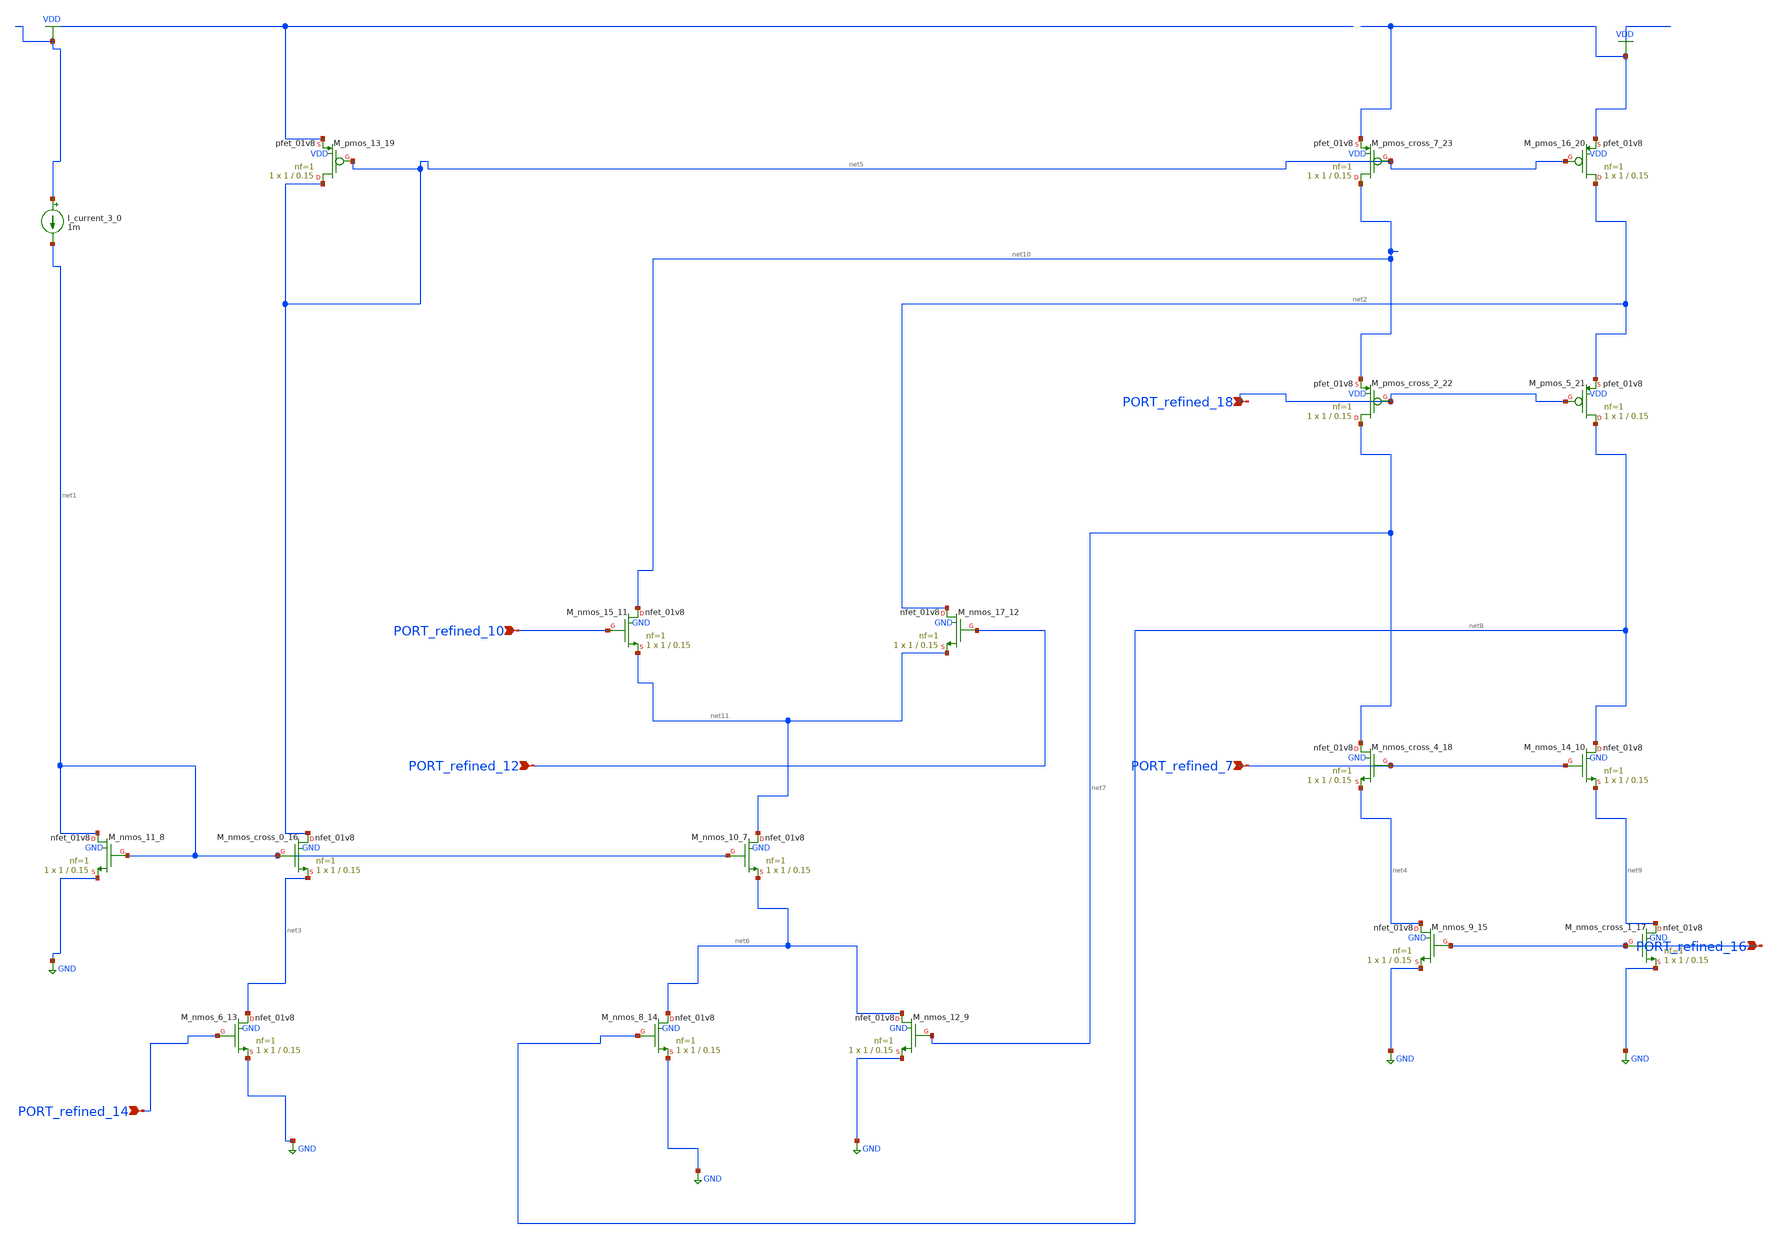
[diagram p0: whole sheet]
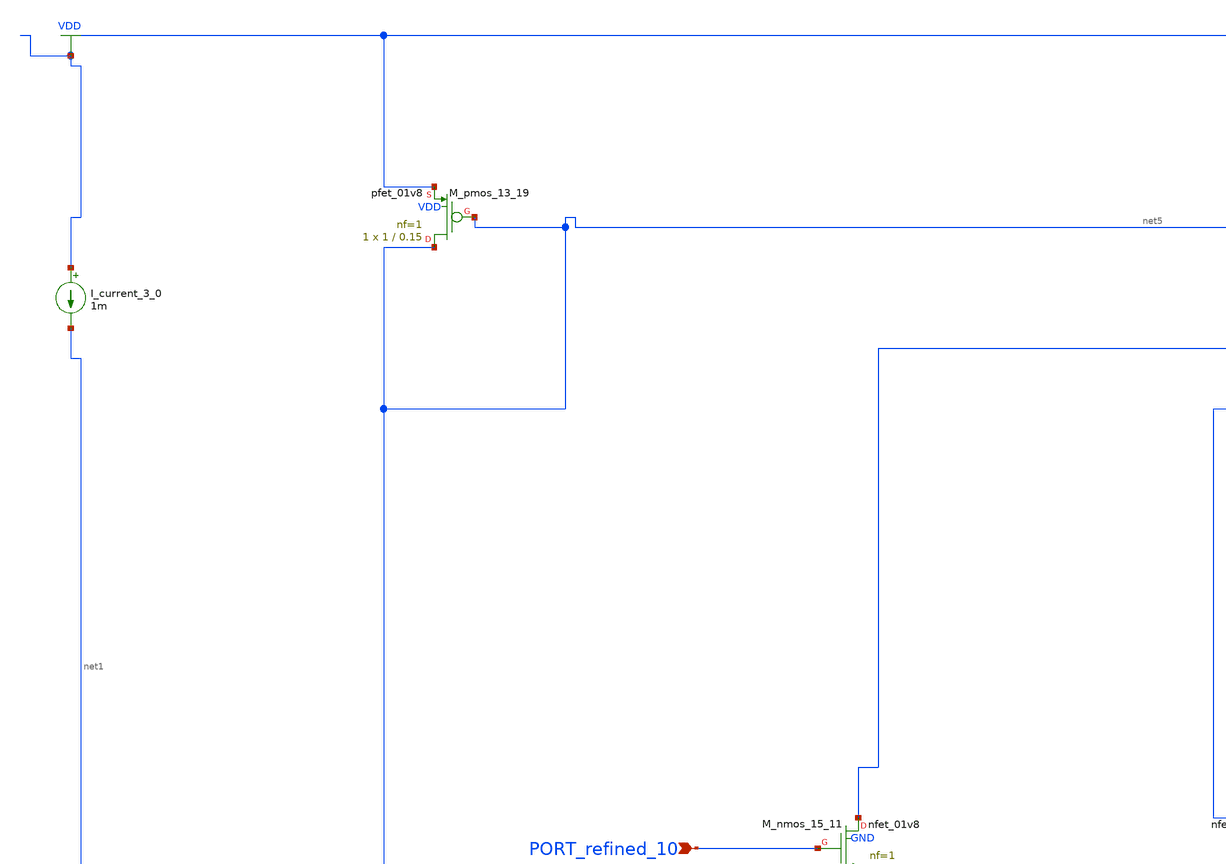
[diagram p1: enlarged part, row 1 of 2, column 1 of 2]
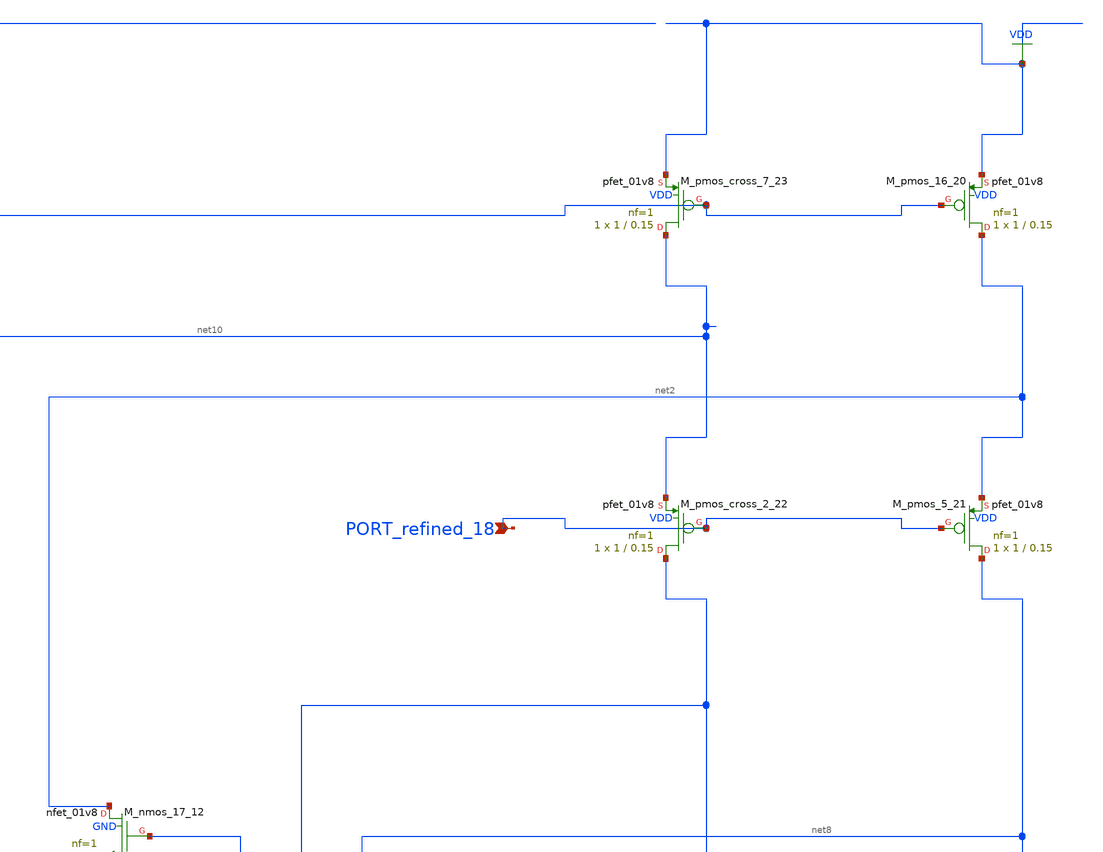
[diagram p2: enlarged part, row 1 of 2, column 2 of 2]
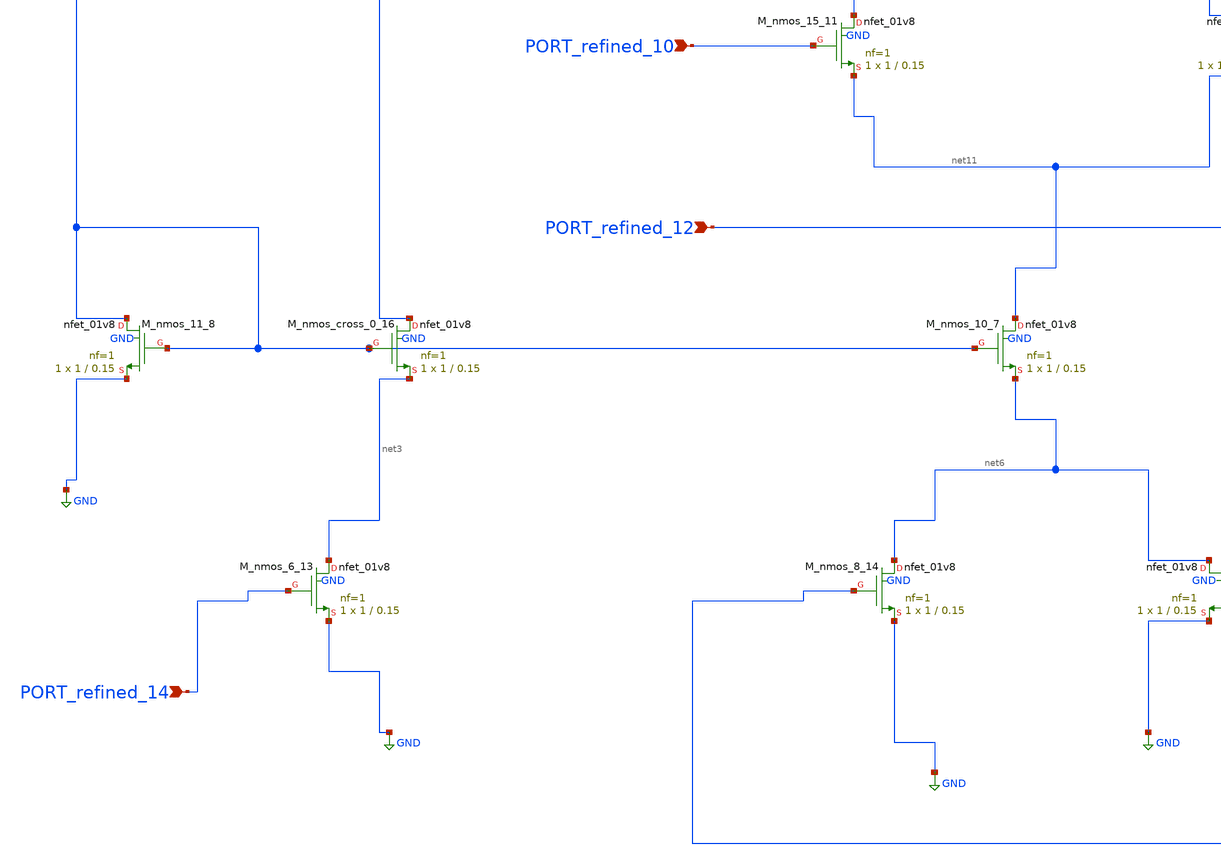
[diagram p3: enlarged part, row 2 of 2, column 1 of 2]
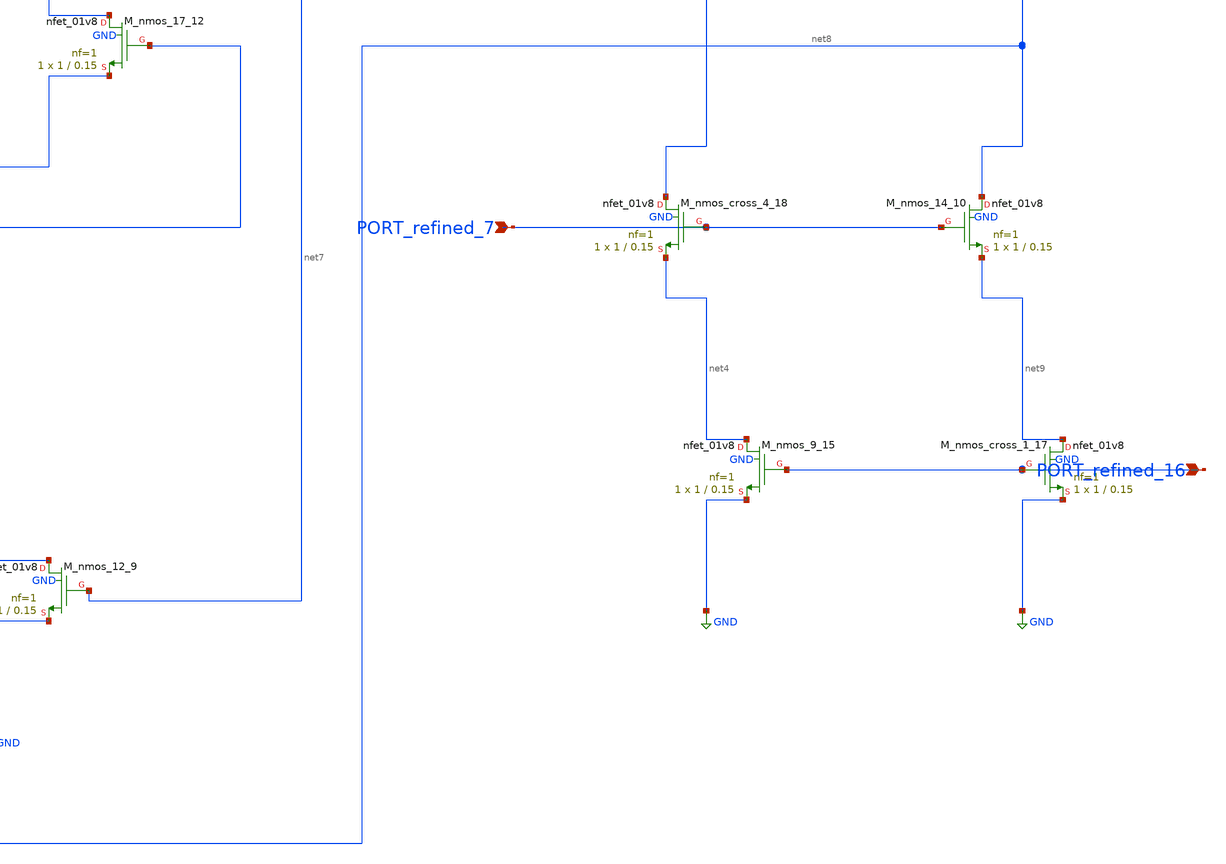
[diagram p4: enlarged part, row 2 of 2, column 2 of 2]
** sch_path: schematics/AMSNet/672.sch
**.subckt 672 PORT_refined_12 PORT_refined_14 PORT_refined_7 PORT_refined_16 PORT_refined_18
*+ PORT_refined_10
*.ipin PORT_refined_12
*.ipin PORT_refined_14
*.ipin PORT_refined_7
*.ipin PORT_refined_16
*.ipin PORT_refined_18
*.ipin PORT_refined_10
I_current_3_0 VDD net1 1m
XM_nmos_10_7 net11 net1 net6 GND sky130_fd_pr__nfet_01v8 L=0.15 W=1 nf=1 ad='int((1 + 1)/2) * 1 / 1 * 0.29'
+ as='int((1 + 2)/2) * 1 / 1 * 0.29' pd='2*int((1 + 1)/2) * (1 / 1 + 0.29)' ps='2*int((1 + 2)/2) * (1 / 1 + 0.29)'
+ nrd='0.29 / 1 ' nrs='0.29 / 1 ' sa=0 sb=0 sd=0 mult=1 m=1
XM_nmos_11_8 net1 net1 GND GND sky130_fd_pr__nfet_01v8 L=0.15 W=1 nf=1 ad='int((1 + 1)/2) * 1 / 1 * 0.29'
+ as='int((1 + 2)/2) * 1 / 1 * 0.29' pd='2*int((1 + 1)/2) * (1 / 1 + 0.29)' ps='2*int((1 + 2)/2) * (1 / 1 + 0.29)'
+ nrd='0.29 / 1 ' nrs='0.29 / 1 ' sa=0 sb=0 sd=0 mult=1 m=1
XM_nmos_12_9 net6 net7 GND GND sky130_fd_pr__nfet_01v8 L=0.15 W=1 nf=1 ad='int((1 + 1)/2) * 1 / 1 * 0.29'
+ as='int((1 + 2)/2) * 1 / 1 * 0.29' pd='2*int((1 + 1)/2) * (1 / 1 + 0.29)' ps='2*int((1 + 2)/2) * (1 / 1 + 0.29)'
+ nrd='0.29 / 1 ' nrs='0.29 / 1 ' sa=0 sb=0 sd=0 mult=1 m=1
XM_nmos_14_10 net8 PORT_refined_7 net9 GND sky130_fd_pr__nfet_01v8 L=0.15 W=1 nf=1 ad='int((1 + 1)/2) * 1 / 1 * 0.29'
+ as='int((1 + 2)/2) * 1 / 1 * 0.29' pd='2*int((1 + 1)/2) * (1 / 1 + 0.29)' ps='2*int((1 + 2)/2) * (1 / 1 + 0.29)'
+ nrd='0.29 / 1 ' nrs='0.29 / 1 ' sa=0 sb=0 sd=0 mult=1 m=1
XM_nmos_15_11 net10 PORT_refined_10 net11 GND sky130_fd_pr__nfet_01v8 L=0.15 W=1 nf=1 ad='int((1 + 1)/2) * 1 / 1 * 0.29'
+ as='int((1 + 2)/2) * 1 / 1 * 0.29' pd='2*int((1 + 1)/2) * (1 / 1 + 0.29)' ps='2*int((1 + 2)/2) * (1 / 1 + 0.29)'
+ nrd='0.29 / 1 ' nrs='0.29 / 1 ' sa=0 sb=0 sd=0 mult=1 m=1
XM_nmos_17_12 net2 PORT_refined_12 net11 GND sky130_fd_pr__nfet_01v8 L=0.15 W=1 nf=1 ad='int((1 + 1)/2) * 1 / 1 * 0.29'
+ as='int((1 + 2)/2) * 1 / 1 * 0.29' pd='2*int((1 + 1)/2) * (1 / 1 + 0.29)' ps='2*int((1 + 2)/2) * (1 / 1 + 0.29)'
+ nrd='0.29 / 1 ' nrs='0.29 / 1 ' sa=0 sb=0 sd=0 mult=1 m=1
XM_nmos_6_13 net3 PORT_refined_14 GND GND sky130_fd_pr__nfet_01v8 L=0.15 W=1 nf=1 ad='int((1 + 1)/2) * 1 / 1 * 0.29'
+ as='int((1 + 2)/2) * 1 / 1 * 0.29' pd='2*int((1 + 1)/2) * (1 / 1 + 0.29)' ps='2*int((1 + 2)/2) * (1 / 1 + 0.29)'
+ nrd='0.29 / 1 ' nrs='0.29 / 1 ' sa=0 sb=0 sd=0 mult=1 m=1
XM_nmos_8_14 net6 net8 GND GND sky130_fd_pr__nfet_01v8 L=0.15 W=1 nf=1 ad='int((1 + 1)/2) * 1 / 1 * 0.29'
+ as='int((1 + 2)/2) * 1 / 1 * 0.29' pd='2*int((1 + 1)/2) * (1 / 1 + 0.29)' ps='2*int((1 + 2)/2) * (1 / 1 + 0.29)'
+ nrd='0.29 / 1 ' nrs='0.29 / 1 ' sa=0 sb=0 sd=0 mult=1 m=1
XM_nmos_9_15 net4 PORT_refined_16 GND GND sky130_fd_pr__nfet_01v8 L=0.15 W=1 nf=1 ad='int((1 + 1)/2) * 1 / 1 * 0.29'
+ as='int((1 + 2)/2) * 1 / 1 * 0.29' pd='2*int((1 + 1)/2) * (1 / 1 + 0.29)' ps='2*int((1 + 2)/2) * (1 / 1 + 0.29)'
+ nrd='0.29 / 1 ' nrs='0.29 / 1 ' sa=0 sb=0 sd=0 mult=1 m=1
XM_nmos_cross_0_16 net5 net1 net3 GND sky130_fd_pr__nfet_01v8 L=0.15 W=1 nf=1 ad='int((1 + 1)/2) * 1 / 1 * 0.29'
+ as='int((1 + 2)/2) * 1 / 1 * 0.29' pd='2*int((1 + 1)/2) * (1 / 1 + 0.29)' ps='2*int((1 + 2)/2) * (1 / 1 + 0.29)'
+ nrd='0.29 / 1 ' nrs='0.29 / 1 ' sa=0 sb=0 sd=0 mult=1 m=1
XM_nmos_cross_1_17 net9 PORT_refined_16 GND GND sky130_fd_pr__nfet_01v8 L=0.15 W=1 nf=1 ad='int((1 + 1)/2) * 1 / 1 * 0.29'
+ as='int((1 + 2)/2) * 1 / 1 * 0.29' pd='2*int((1 + 1)/2) * (1 / 1 + 0.29)' ps='2*int((1 + 2)/2) * (1 / 1 + 0.29)'
+ nrd='0.29 / 1 ' nrs='0.29 / 1 ' sa=0 sb=0 sd=0 mult=1 m=1
XM_nmos_cross_4_18 net7 PORT_refined_7 net4 GND sky130_fd_pr__nfet_01v8 L=0.15 W=1 nf=1 ad='int((1 + 1)/2) * 1 / 1 * 0.29'
+ as='int((1 + 2)/2) * 1 / 1 * 0.29' pd='2*int((1 + 1)/2) * (1 / 1 + 0.29)' ps='2*int((1 + 2)/2) * (1 / 1 + 0.29)'
+ nrd='0.29 / 1 ' nrs='0.29 / 1 ' sa=0 sb=0 sd=0 mult=1 m=1
XM_pmos_13_19 net5 net5 VDD VDD sky130_fd_pr__pfet_01v8 L=0.15 W=1 nf=1 ad='int((1 + 1)/2) * 1 / 1 * 0.29'
+ as='int((1 + 2)/2) * 1 / 1 * 0.29' pd='2*int((1 + 1)/2) * (1 / 1 + 0.29)' ps='2*int((1 + 2)/2) * (1 / 1 + 0.29)'
+ nrd='0.29 / 1 ' nrs='0.29 / 1 ' sa=0 sb=0 sd=0 mult=1 m=1
XM_pmos_16_20 net2 net5 VDD VDD sky130_fd_pr__pfet_01v8 L=0.15 W=1 nf=1 ad='int((1 + 1)/2) * 1 / 1 * 0.29'
+ as='int((1 + 2)/2) * 1 / 1 * 0.29' pd='2*int((1 + 1)/2) * (1 / 1 + 0.29)' ps='2*int((1 + 2)/2) * (1 / 1 + 0.29)'
+ nrd='0.29 / 1 ' nrs='0.29 / 1 ' sa=0 sb=0 sd=0 mult=1 m=1
XM_pmos_5_21 net8 PORT_refined_18 net2 VDD sky130_fd_pr__pfet_01v8 L=0.15 W=1 nf=1 ad='int((1 + 1)/2) * 1 / 1 * 0.29'
+ as='int((1 + 2)/2) * 1 / 1 * 0.29' pd='2*int((1 + 1)/2) * (1 / 1 + 0.29)' ps='2*int((1 + 2)/2) * (1 / 1 + 0.29)'
+ nrd='0.29 / 1 ' nrs='0.29 / 1 ' sa=0 sb=0 sd=0 mult=1 m=1
XM_pmos_cross_2_22 net7 PORT_refined_18 net10 VDD sky130_fd_pr__pfet_01v8 L=0.15 W=1 nf=1 ad='int((1 + 1)/2) * 1 / 1 * 0.29'
+ as='int((1 + 2)/2) * 1 / 1 * 0.29' pd='2*int((1 + 1)/2) * (1 / 1 + 0.29)' ps='2*int((1 + 2)/2) * (1 / 1 + 0.29)'
+ nrd='0.29 / 1 ' nrs='0.29 / 1 ' sa=0 sb=0 sd=0 mult=1 m=1
XM_pmos_cross_7_23 net10 net5 VDD VDD sky130_fd_pr__pfet_01v8 L=0.15 W=1 nf=1 ad='int((1 + 1)/2) * 1 / 1 * 0.29'
+ as='int((1 + 2)/2) * 1 / 1 * 0.29' pd='2*int((1 + 1)/2) * (1 / 1 + 0.29)' ps='2*int((1 + 2)/2) * (1 / 1 + 0.29)'
+ nrd='0.29 / 1 ' nrs='0.29 / 1 ' sa=0 sb=0 sd=0 mult=1 m=1
**.ends
.GLOBAL GND
.GLOBAL VDD
.end
